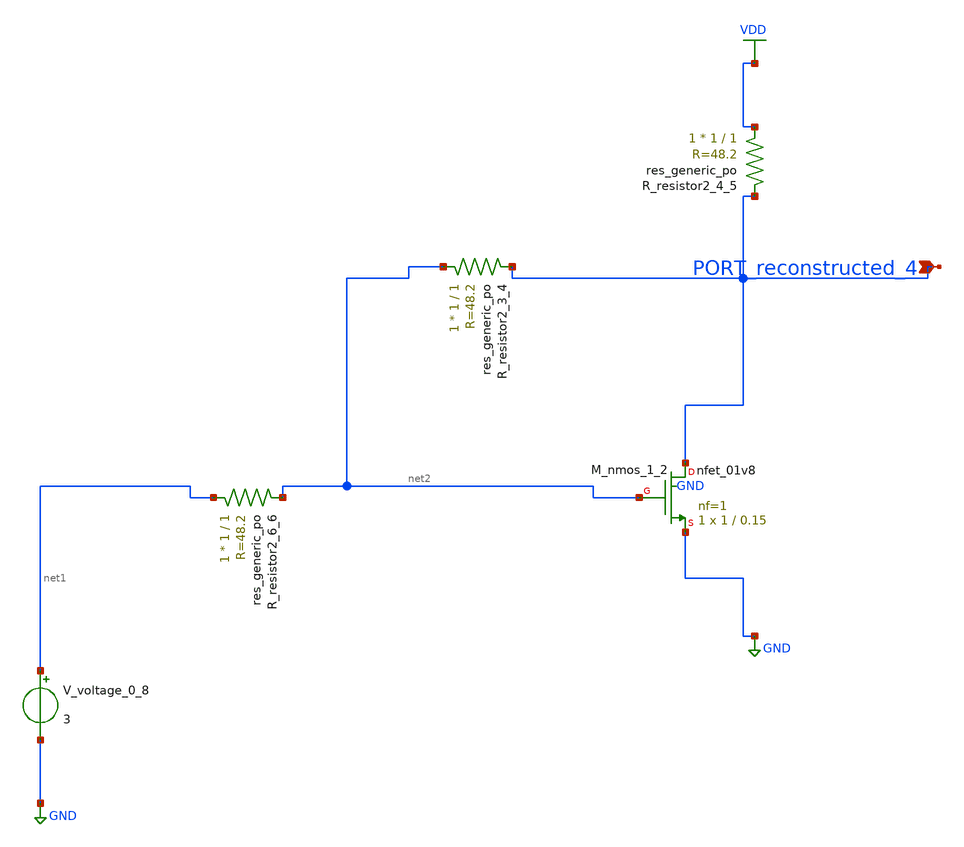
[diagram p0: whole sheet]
** sch_path: schematics/AMSNet/585.sch
**.subckt 585 PORT_reconstructed_4
*.ipin PORT_reconstructed_4
XM_nmos_1_2 PORT_reconstructed_4 net2 GND GND sky130_fd_pr__nfet_01v8 L=0.15 W=1 nf=1 ad='int((1 + 1)/2) * 1 / 1 * 0.29'
+ as='int((1 + 2)/2) * 1 / 1 * 0.29' pd='2*int((1 + 1)/2) * (1 / 1 + 0.29)' ps='2*int((1 + 2)/2) * (1 / 1 + 0.29)'
+ nrd='0.29 / 1 ' nrs='0.29 / 1 ' sa=0 sb=0 sd=0 mult=1 m=1
XR_resistor2_3_4 net2 PORT_reconstructed_4 sky130_fd_pr__res_generic_po W=1 L=1 m=1
XR_resistor2_4_5 VDD PORT_reconstructed_4 sky130_fd_pr__res_generic_po W=1 L=1 m=1
XR_resistor2_6_6 net1 net2 sky130_fd_pr__res_generic_po W=1 L=1 m=1
V_voltage_0_8 net1 GND 3
**.ends
.GLOBAL GND
.GLOBAL VDD
.end
